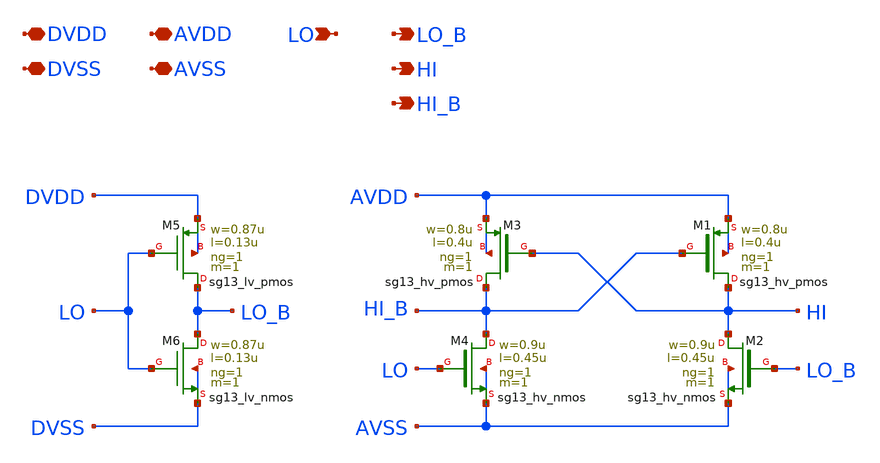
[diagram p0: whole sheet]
** sch_path: xschem/level_shifter_xd.sch
**.subckt level_shifter_xd DVDD DVSS AVDD AVSS LO LO_B HI HI_B
*.iopin DVDD
*.iopin DVSS
*.iopin AVDD
*.iopin AVSS
*.ipin LO
*.opin LO_B
*.opin HI
*.opin HI_B
XM1 HI HI_B AVDD AVDD sg13_hv_pmos w=0.8u l=0.4u ng=1 m=1 mm_ok=1
XM2 HI LO_B AVSS AVSS sg13_hv_nmos w=0.9u l=0.45u ng=1 m=1 mm_ok=1
XM3 HI_B HI AVDD AVDD sg13_hv_pmos w=0.8u l=0.4u ng=1 m=1 mm_ok=1
XM4 HI_B LO AVSS AVSS sg13_hv_nmos w=0.9u l=0.45u ng=1 m=1 mm_ok=1
XM5 LO_B LO DVDD DVDD sg13_lv_pmos w=0.87u l=0.13u ng=1 m=1 mm_ok=1
XM6 LO_B LO DVSS DVSS sg13_lv_nmos w=0.87u l=0.13u ng=1 m=1 mm_ok=1
**.ends
.end
